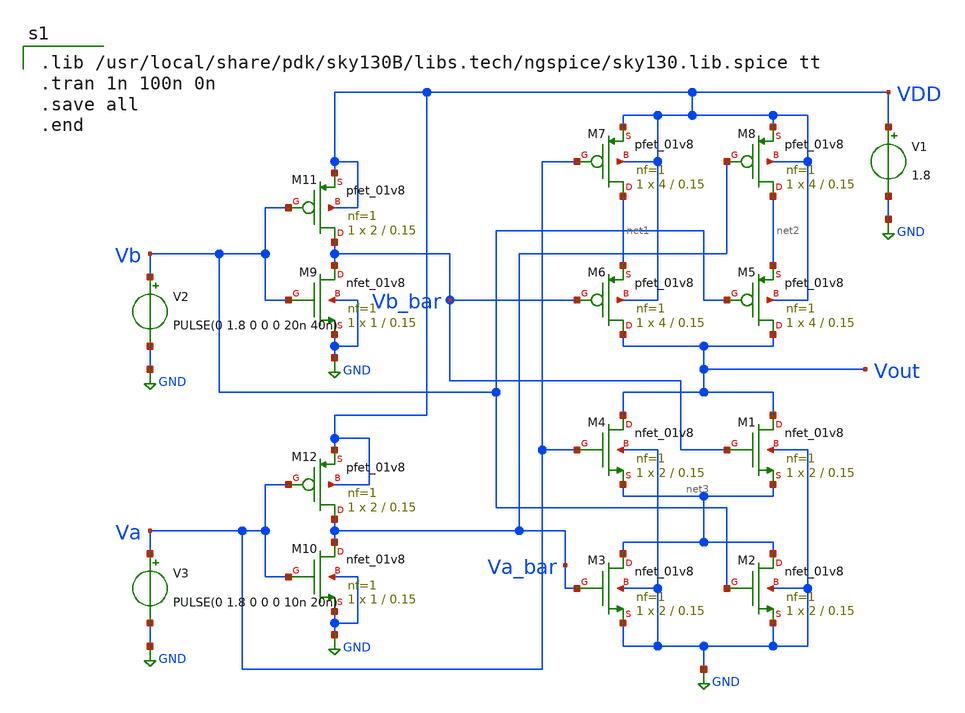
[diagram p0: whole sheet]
** sch_path: physical_design_layout_of_2_input_xor_gate/xor2gate.sch
**.subckt xor2gate
XM1 Vout Vb_bar net3 GND sky130_fd_pr__nfet_01v8 L=0.15 W=2 nf=1 ad='int((nf+1)/2) * W/nf * 0.29' as='int((nf+2)/2) * W/nf * 0.29'
+ pd='2*int((nf+1)/2) * (W/nf + 0.29)' ps='2*int((nf+2)/2) * (W/nf + 0.29)' nrd='0.29 / W' nrs='0.29 / W'
+ sa=0 sb=0 sd=0 mult=1 m=1
XM2 net3 Vb GND GND sky130_fd_pr__nfet_01v8 L=0.15 W=2 nf=1 ad='int((nf+1)/2) * W/nf * 0.29' as='int((nf+2)/2) * W/nf * 0.29'
+ pd='2*int((nf+1)/2) * (W/nf + 0.29)' ps='2*int((nf+2)/2) * (W/nf + 0.29)' nrd='0.29 / W' nrs='0.29 / W'
+ sa=0 sb=0 sd=0 mult=1 m=1
XM3 net3 Va_bar GND GND sky130_fd_pr__nfet_01v8 L=0.15 W=2 nf=1 ad='int((nf+1)/2) * W/nf * 0.29' as='int((nf+2)/2) * W/nf * 0.29'
+ pd='2*int((nf+1)/2) * (W/nf + 0.29)' ps='2*int((nf+2)/2) * (W/nf + 0.29)' nrd='0.29 / W' nrs='0.29 / W'
+ sa=0 sb=0 sd=0 mult=1 m=1
XM4 Vout Va net3 GND sky130_fd_pr__nfet_01v8 L=0.15 W=2 nf=1 ad='int((nf+1)/2) * W/nf * 0.29' as='int((nf+2)/2) * W/nf * 0.29'
+ pd='2*int((nf+1)/2) * (W/nf + 0.29)' ps='2*int((nf+2)/2) * (W/nf + 0.29)' nrd='0.29 / W' nrs='0.29 / W'
+ sa=0 sb=0 sd=0 mult=1 m=1
XM5 Vout Vb net2 VDD sky130_fd_pr__pfet_01v8 L=0.15 W=4 nf=1 ad='int((nf+1)/2) * W/nf * 0.29' as='int((nf+2)/2) * W/nf * 0.29'
+ pd='2*int((nf+1)/2) * (W/nf + 0.29)' ps='2*int((nf+2)/2) * (W/nf + 0.29)' nrd='0.29 / W' nrs='0.29 / W'
+ sa=0 sb=0 sd=0 mult=1 m=1
XM6 Vout Vb_bar net1 VDD sky130_fd_pr__pfet_01v8 L=0.15 W=4 nf=1 ad='int((nf+1)/2) * W/nf * 0.29' as='int((nf+2)/2) * W/nf * 0.29'
+ pd='2*int((nf+1)/2) * (W/nf + 0.29)' ps='2*int((nf+2)/2) * (W/nf + 0.29)' nrd='0.29 / W' nrs='0.29 / W'
+ sa=0 sb=0 sd=0 mult=1 m=1
XM7 net1 Va VDD VDD sky130_fd_pr__pfet_01v8 L=0.15 W=4 nf=1 ad='int((nf+1)/2) * W/nf * 0.29' as='int((nf+2)/2) * W/nf * 0.29'
+ pd='2*int((nf+1)/2) * (W/nf + 0.29)' ps='2*int((nf+2)/2) * (W/nf + 0.29)' nrd='0.29 / W' nrs='0.29 / W'
+ sa=0 sb=0 sd=0 mult=1 m=1
XM8 net2 Va_bar VDD VDD sky130_fd_pr__pfet_01v8 L=0.15 W=4 nf=1 ad='int((nf+1)/2) * W/nf * 0.29' as='int((nf+2)/2) * W/nf * 0.29'
+ pd='2*int((nf+1)/2) * (W/nf + 0.29)' ps='2*int((nf+2)/2) * (W/nf + 0.29)' nrd='0.29 / W' nrs='0.29 / W'
+ sa=0 sb=0 sd=0 mult=1 m=1
XM9 Vb_bar Vb GND GND sky130_fd_pr__nfet_01v8 L=0.15 W=1 nf=1 ad='int((nf+1)/2) * W/nf * 0.29' as='int((nf+2)/2) * W/nf * 0.29'
+ pd='2*int((nf+1)/2) * (W/nf + 0.29)' ps='2*int((nf+2)/2) * (W/nf + 0.29)' nrd='0.29 / W' nrs='0.29 / W'
+ sa=0 sb=0 sd=0 mult=1 m=1
XM10 Va_bar Va GND GND sky130_fd_pr__nfet_01v8 L=0.15 W=1 nf=1 ad='int((nf+1)/2) * W/nf * 0.29' as='int((nf+2)/2) * W/nf * 0.29'
+ pd='2*int((nf+1)/2) * (W/nf + 0.29)' ps='2*int((nf+2)/2) * (W/nf + 0.29)' nrd='0.29 / W' nrs='0.29 / W'
+ sa=0 sb=0 sd=0 mult=1 m=1
XM11 Vb_bar Vb VDD VDD sky130_fd_pr__pfet_01v8 L=0.15 W=2 nf=1 ad='int((nf+1)/2) * W/nf * 0.29' as='int((nf+2)/2) * W/nf * 0.29'
+ pd='2*int((nf+1)/2) * (W/nf + 0.29)' ps='2*int((nf+2)/2) * (W/nf + 0.29)' nrd='0.29 / W' nrs='0.29 / W'
+ sa=0 sb=0 sd=0 mult=1 m=1
XM12 Va_bar Va VDD VDD sky130_fd_pr__pfet_01v8 L=0.15 W=2 nf=1 ad='int((nf+1)/2) * W/nf * 0.29' as='int((nf+2)/2) * W/nf * 0.29'
+ pd='2*int((nf+1)/2) * (W/nf + 0.29)' ps='2*int((nf+2)/2) * (W/nf + 0.29)' nrd='0.29 / W' nrs='0.29 / W'
+ sa=0 sb=0 sd=0 mult=1 m=1
V1 VDD GND 1.8
V2 Vb GND PULSE(0 1.8 0 0 0 20n 40n)
V3 Va GND PULSE(0 1.8 0 0 0 10n 20n)
**** begin user architecture code

.lib /usr/local/share/pdk/sky130B/libs.tech/ngspice/sky130.lib.spice tt
.tran 1n 100n 0n
.save all
.end

**** end user architecture code
**.ends
.GLOBAL GND
.end
